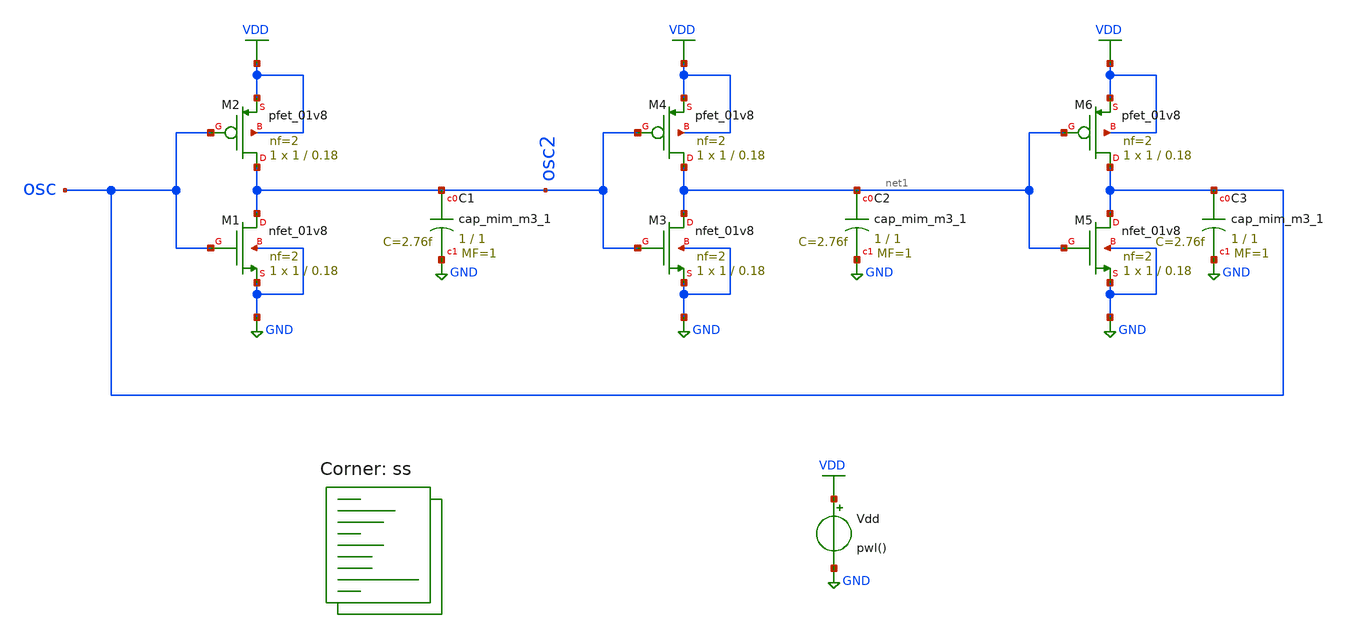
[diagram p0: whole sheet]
** sch_path: projects/bandgapref/xschem_ngspice/old_files/test_inverter_speed.sch
**.subckt test_inverter_speed
XM1 osc2 osc GND GND sky130_fd_pr__nfet_01v8 L=0.18 W=1 nf=2 ad='int((nf+1)/2) * W/nf * 0.29' as='int((nf+2)/2) * W/nf * 0.29'
+ pd='2*int((nf+1)/2) * (W/nf + 0.29)' ps='2*int((nf+2)/2) * (W/nf + 0.29)' nrd='0.29 / W' nrs='0.29 / W'
+ sa=0 sb=0 sd=0 mult=1 m=1
XC1 osc2 GND sky130_fd_pr__cap_mim_m3_1 W=1 L=1 MF=1 m=1
XC2 net1 GND sky130_fd_pr__cap_mim_m3_1 W=1 L=1 MF=1 m=1
XC3 osc GND sky130_fd_pr__cap_mim_m3_1 W=1 L=1 MF=1 m=1
XM2 osc2 osc VDD VDD sky130_fd_pr__pfet_01v8 L=0.18 W=1 nf=2 ad='int((nf+1)/2) * W/nf * 0.29' as='int((nf+2)/2) * W/nf * 0.29'
+ pd='2*int((nf+1)/2) * (W/nf + 0.29)' ps='2*int((nf+2)/2) * (W/nf + 0.29)' nrd='0.29 / W' nrs='0.29 / W'
+ sa=0 sb=0 sd=0 mult=1 m=1
XM3 net1 osc2 GND GND sky130_fd_pr__nfet_01v8 L=0.18 W=1 nf=2 ad='int((nf+1)/2) * W/nf * 0.29' as='int((nf+2)/2) * W/nf * 0.29'
+ pd='2*int((nf+1)/2) * (W/nf + 0.29)' ps='2*int((nf+2)/2) * (W/nf + 0.29)' nrd='0.29 / W' nrs='0.29 / W'
+ sa=0 sb=0 sd=0 mult=1 m=1
XM4 net1 osc2 VDD VDD sky130_fd_pr__pfet_01v8 L=0.18 W=1 nf=2 ad='int((nf+1)/2) * W/nf * 0.29' as='int((nf+2)/2) * W/nf * 0.29'
+ pd='2*int((nf+1)/2) * (W/nf + 0.29)' ps='2*int((nf+2)/2) * (W/nf + 0.29)' nrd='0.29 / W' nrs='0.29 / W'
+ sa=0 sb=0 sd=0 mult=1 m=1
XM5 osc net1 GND GND sky130_fd_pr__nfet_01v8 L=0.18 W=1 nf=2 ad='int((nf+1)/2) * W/nf * 0.29' as='int((nf+2)/2) * W/nf * 0.29'
+ pd='2*int((nf+1)/2) * (W/nf + 0.29)' ps='2*int((nf+2)/2) * (W/nf + 0.29)' nrd='0.29 / W' nrs='0.29 / W'
+ sa=0 sb=0 sd=0 mult=1 m=1
XM6 osc net1 VDD VDD sky130_fd_pr__pfet_01v8 L=0.18 W=1 nf=2 ad='int((nf+1)/2) * W/nf * 0.29' as='int((nf+2)/2) * W/nf * 0.29'
+ pd='2*int((nf+1)/2) * (W/nf + 0.29)' ps='2*int((nf+2)/2) * (W/nf + 0.29)' nrd='0.29 / W' nrs='0.29 / W'
+ sa=0 sb=0 sd=0 mult=1 m=1
Vdd VDD GND pwl()
**** begin user architecture code
.lib $::SKYWATER_MODELS/sky130.lib.spice ss



.option method=gear
.option wnflag=1
.option savecurrents


.save @m.xm1.msky130_fd_pr__nfet_01v8[gm] @m.xm2.msky130_fd_pr__pfet_01v8[gm] @m.xm3.msky130_fd_pr__nfet_01v8[gm] @m.xm4.msky130_fd_pr__pfet_01v8[gm] @m.xm5.msky130_fd_pr__nfet_01v8[gm] @m.xm6.msky130_fd_pr__pfet_01v8[gm]

.temp 75
.ic v(osc)=0

.control
  save all
  tran 1ps 30ns
  remzerovec
  linearize v(osc) v(vdd)
  write test_inverter_speed.raw
  wrdata /foss/designs/my_design/projects/pll/bandgapref/xschem_ngspice/oscillator.txt v(osc)
  set appendwrite
.endc




**** end user architecture code
**.ends
.GLOBAL GND
.GLOBAL VDD
.end
